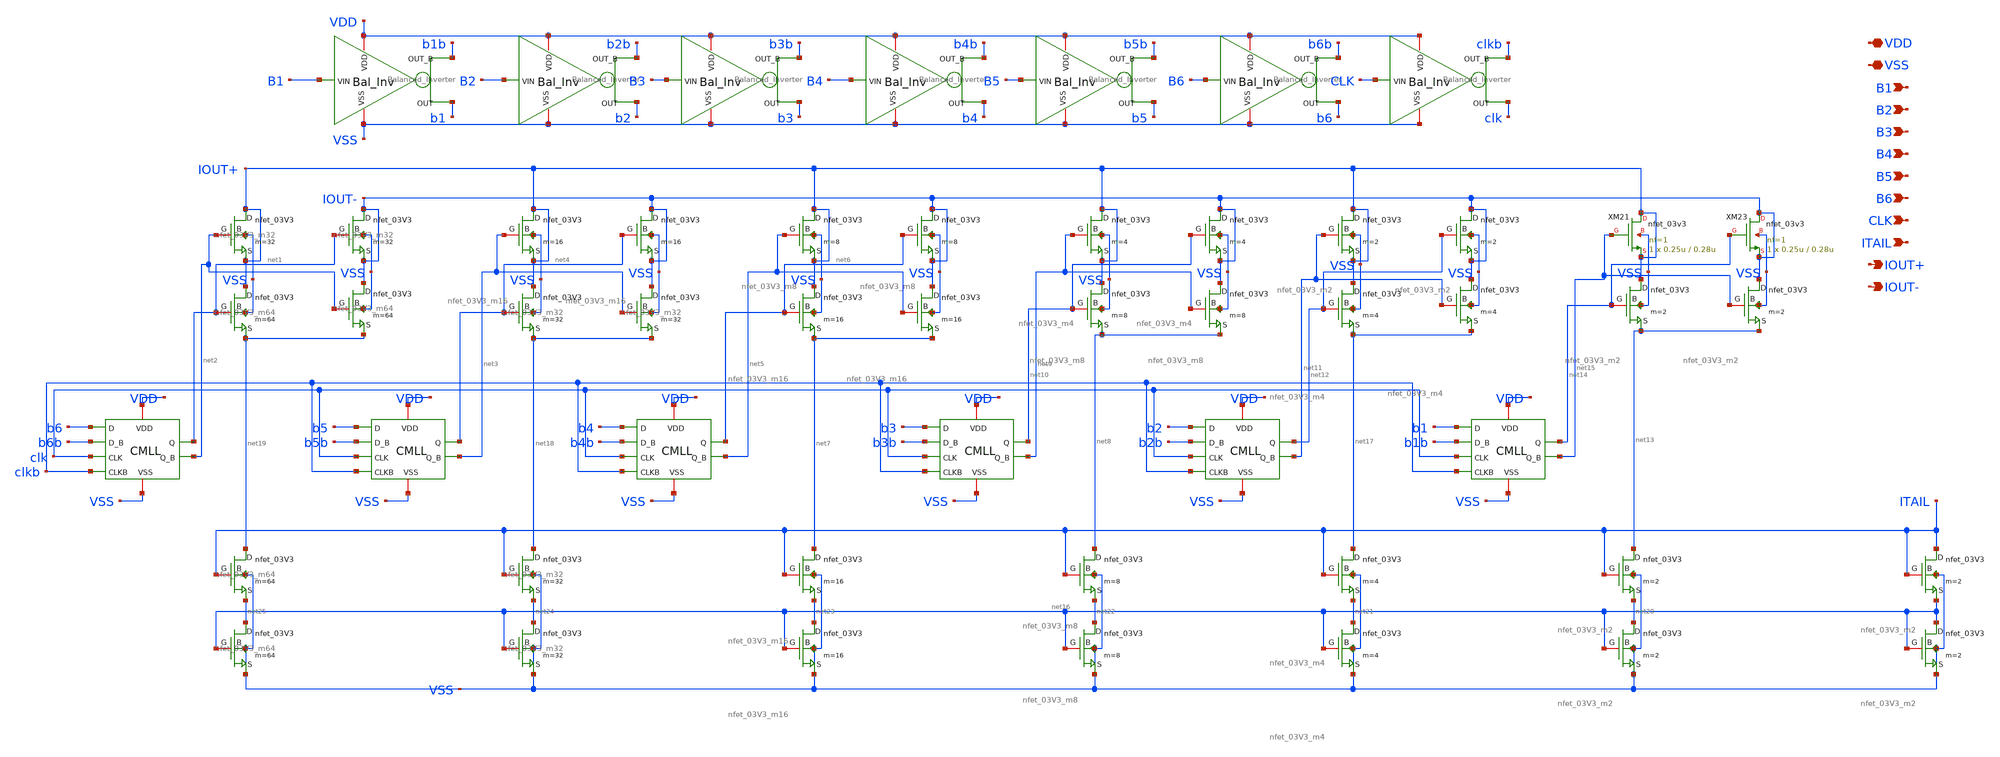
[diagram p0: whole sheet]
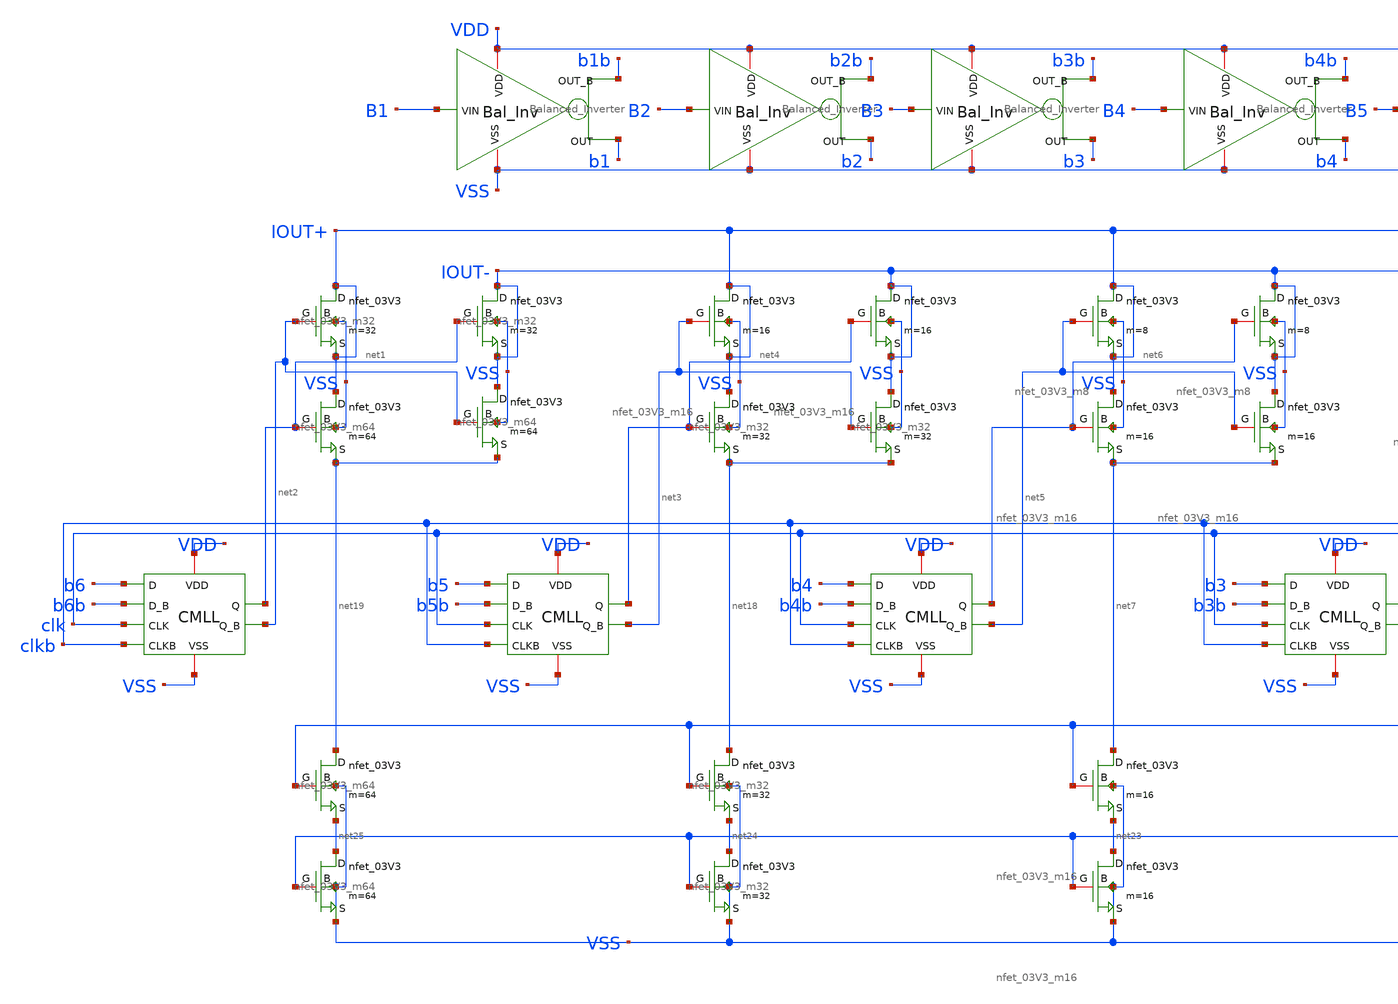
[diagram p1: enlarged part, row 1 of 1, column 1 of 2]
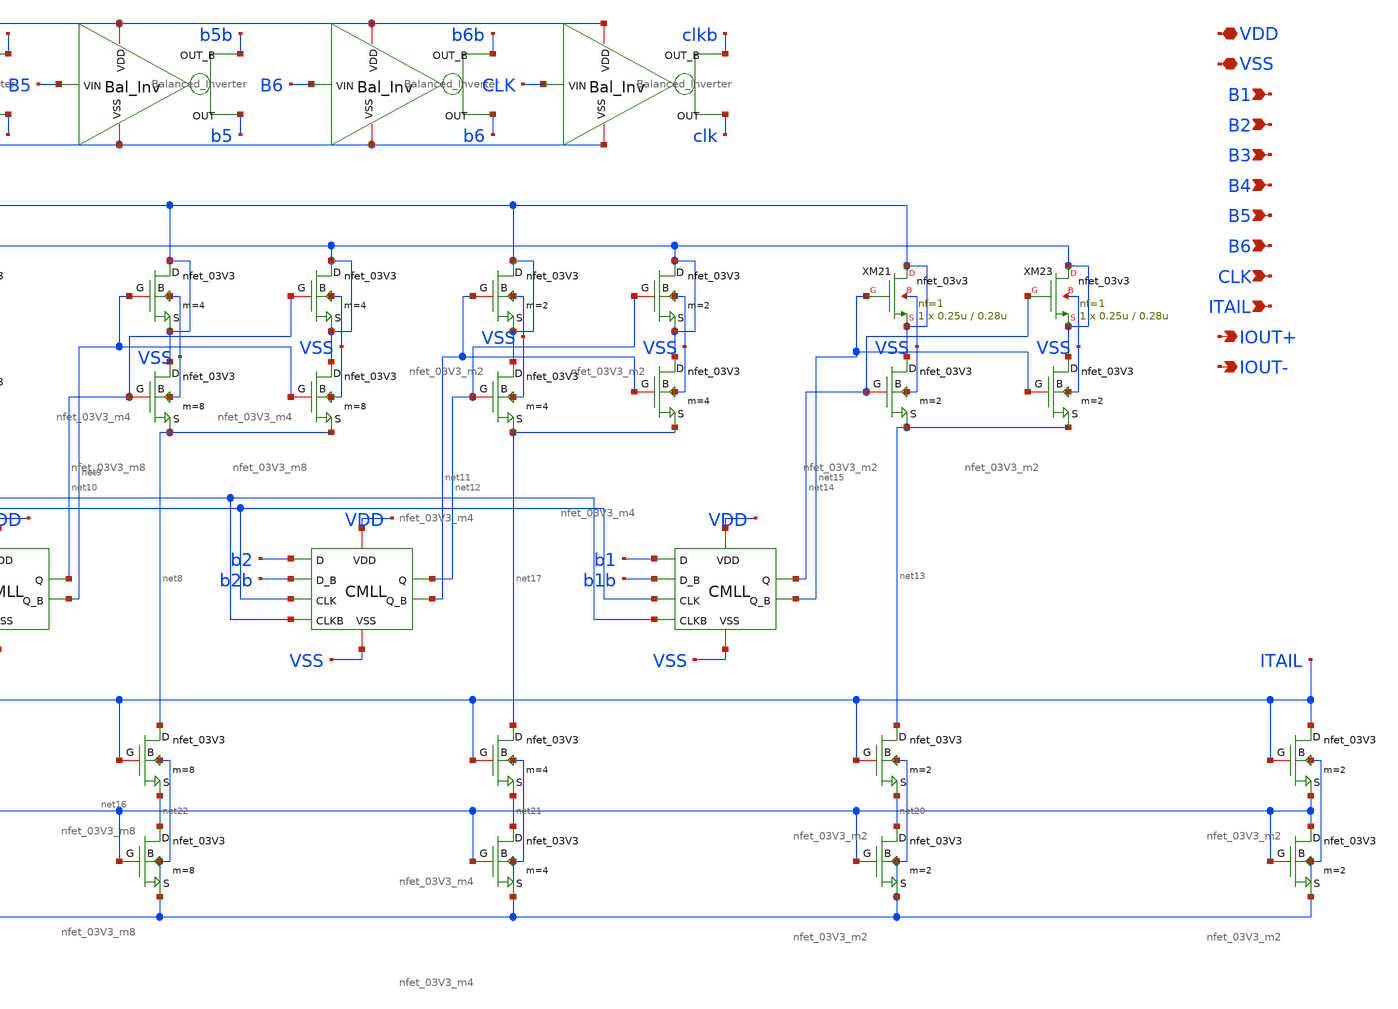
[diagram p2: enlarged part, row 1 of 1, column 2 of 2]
** sch_path: DAC_PAKISTAN_01/Pakistan1_Xschem/LSB.sch
**.subckt LSB VDD VSS B1 B2 B3 B4 B5 B6 CLK ITAIL IOUT+ IOUT-
*.iopin VDD
*.iopin VSS
*.ipin B1
*.ipin B2
*.ipin B3
*.ipin B4
*.ipin B5
*.ipin B6
*.ipin CLK
*.ipin ITAIL
*.opin IOUT+
*.opin IOUT-
x1 VDD VSS B1 b1b b1 Balanced_Inverter
x2 VDD VSS B2 b2b b2 Balanced_Inverter
x3 VDD VSS B3 b3b b3 Balanced_Inverter
x4 VDD VSS B4 b4b b4 Balanced_Inverter
x5 VDD VSS B5 b5b b5 Balanced_Inverter
x6 VDD VSS B6 b6b b6 Balanced_Inverter
x7 VDD VSS CLK clkb clk Balanced_Inverter
XM21 IOUT+ net15 IOUT+ VSS nfet_03v3 L=0.28u W=0.25u nf=1 ad='int((nf+1)/2) * W/nf * 0.18u' as='int((nf+2)/2) * W/nf * 0.18u'
+ pd='2*int((nf+1)/2) * (W/nf + 0.18u)' ps='2*int((nf+2)/2) * (W/nf + 0.18u)' nrd='0.18u / W' nrs='0.18u / W'
+ sa=0 sb=0 sd=0 m=1
x9 VDD VSS b5 b5b clk clkb net4 net3 CMLL
x10 VDD VSS b4 b4b clk clkb net6 net5 CMLL
x11 VDD VSS b3 b3b clk clkb net10 net9 CMLL
x12 VDD VSS b2 b2b clk clkb net12 net11 CMLL
x13 VDD VSS b1 b1b clk clkb net14 net15 CMLL
x14 VDD VSS b6 b6b clk clkb net1 net2 CMLL
XM23 IOUT- net14 IOUT- VSS nfet_03v3 L=0.28u W=0.25u nf=1 ad='int((nf+1)/2) * W/nf * 0.18u' as='int((nf+2)/2) * W/nf * 0.18u'
+ pd='2*int((nf+1)/2) * (W/nf + 0.18u)' ps='2*int((nf+2)/2) * (W/nf + 0.18u)' nrd='0.18u / W' nrs='0.18u / W'
+ sa=0 sb=0 sd=0 m=1
x8 net13 IOUT- VSS net15 nfet_03V3_m2
x15 net13 IOUT+ VSS net14 nfet_03V3_m2
x16 net16 ITAIL VSS ITAIL nfet_03V3_m2
x17 VSS net16 VSS net16 nfet_03V3_m2
x18 net20 net13 VSS ITAIL nfet_03V3_m2
x19 VSS net20 VSS net16 nfet_03V3_m2
x20 IOUT+ IOUT+ VSS net11 nfet_03V3_m2
x21 IOUT- IOUT- VSS net12 nfet_03V3_m2
x22 net17 IOUT+ VSS net12 nfet_03V3_m4
x23 net17 IOUT- VSS net11 nfet_03V3_m4
x24 IOUT+ IOUT+ VSS net9 nfet_03V3_m4
x25 IOUT- IOUT- VSS net10 nfet_03V3_m4
x26 net21 net17 VSS ITAIL nfet_03V3_m4
x27 VSS net21 VSS net16 nfet_03V3_m4
x28 net22 net8 VSS ITAIL nfet_03V3_m8
x29 VSS net22 VSS net16 nfet_03V3_m8
x30 net8 IOUT- VSS net9 nfet_03V3_m8
x31 net8 IOUT+ VSS net10 nfet_03V3_m8
x32 IOUT- IOUT- VSS net6 nfet_03V3_m8
x33 IOUT+ IOUT+ VSS net5 nfet_03V3_m8
x34 net7 IOUT- VSS net5 nfet_03V3_m16
x35 net7 IOUT+ VSS net6 nfet_03V3_m16
x36 IOUT- IOUT- VSS net4 nfet_03V3_m16
x37 IOUT+ IOUT+ VSS net3 nfet_03V3_m16
x38 net23 net7 VSS ITAIL nfet_03V3_m16
x39 VSS net23 VSS net16 nfet_03V3_m16
x40 net24 net18 VSS ITAIL nfet_03V3_m32
x41 VSS net24 VSS net16 nfet_03V3_m32
x42 net18 IOUT- VSS net3 nfet_03V3_m32
x43 net18 IOUT+ VSS net4 nfet_03V3_m32
x44 IOUT- IOUT- VSS net1 nfet_03V3_m32
x45 IOUT+ IOUT+ VSS net2 nfet_03V3_m32
x46 net25 net19 VSS ITAIL nfet_03V3_m64
x47 VSS net25 VSS net16 nfet_03V3_m64
x48 net19 IOUT- VSS net2 nfet_03V3_m64
x49 net19 IOUT+ VSS net1 nfet_03V3_m64
**.ends
.end
